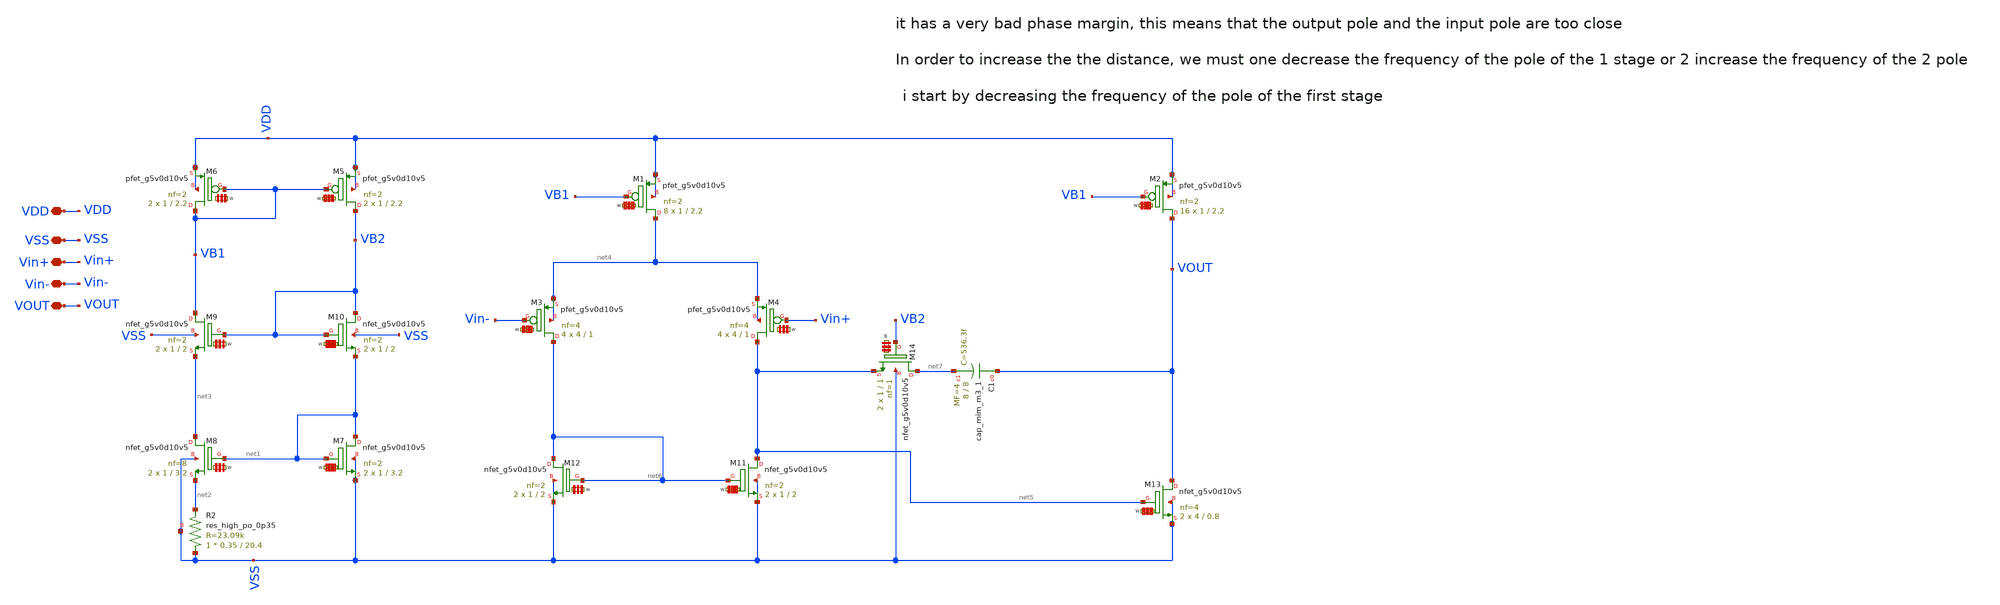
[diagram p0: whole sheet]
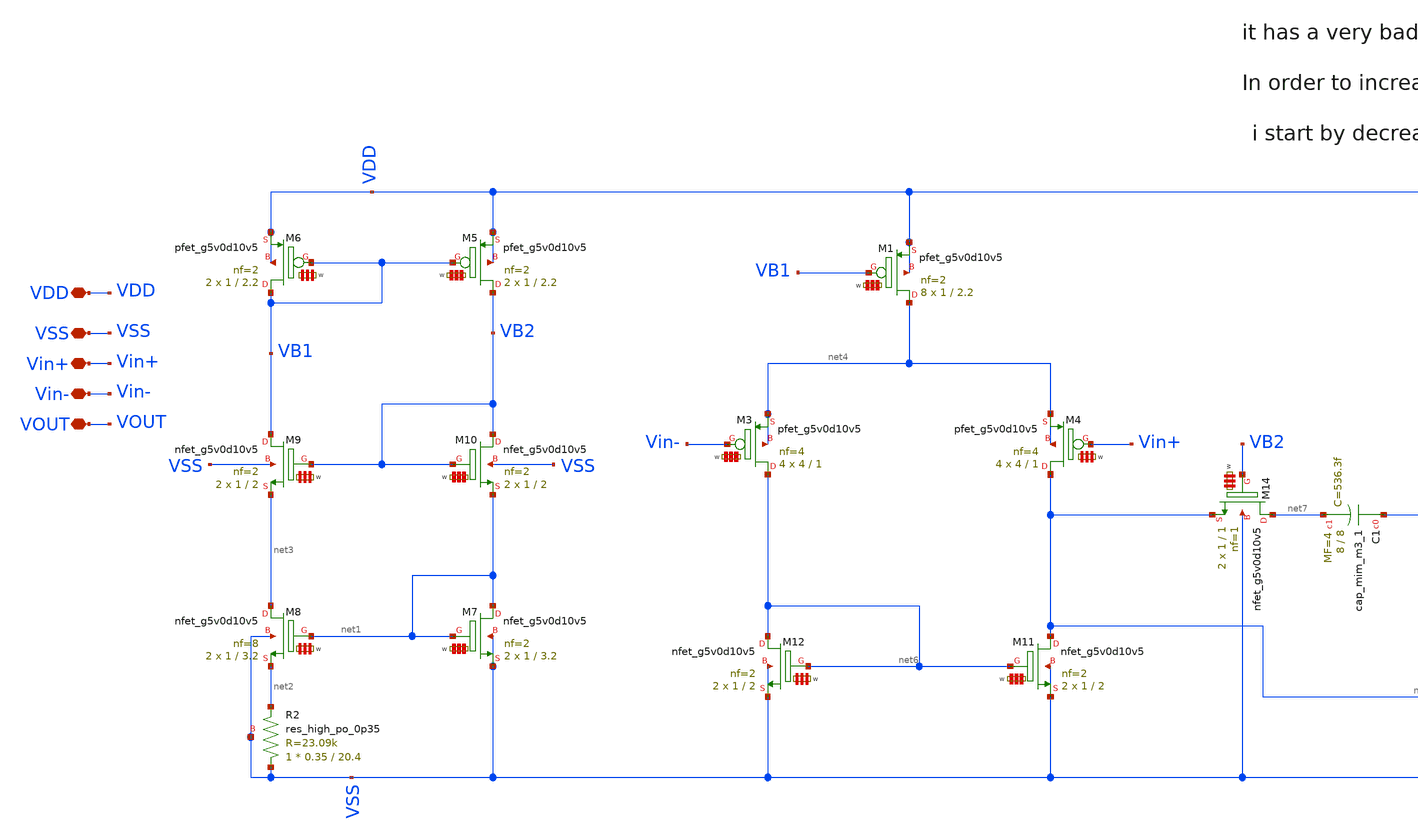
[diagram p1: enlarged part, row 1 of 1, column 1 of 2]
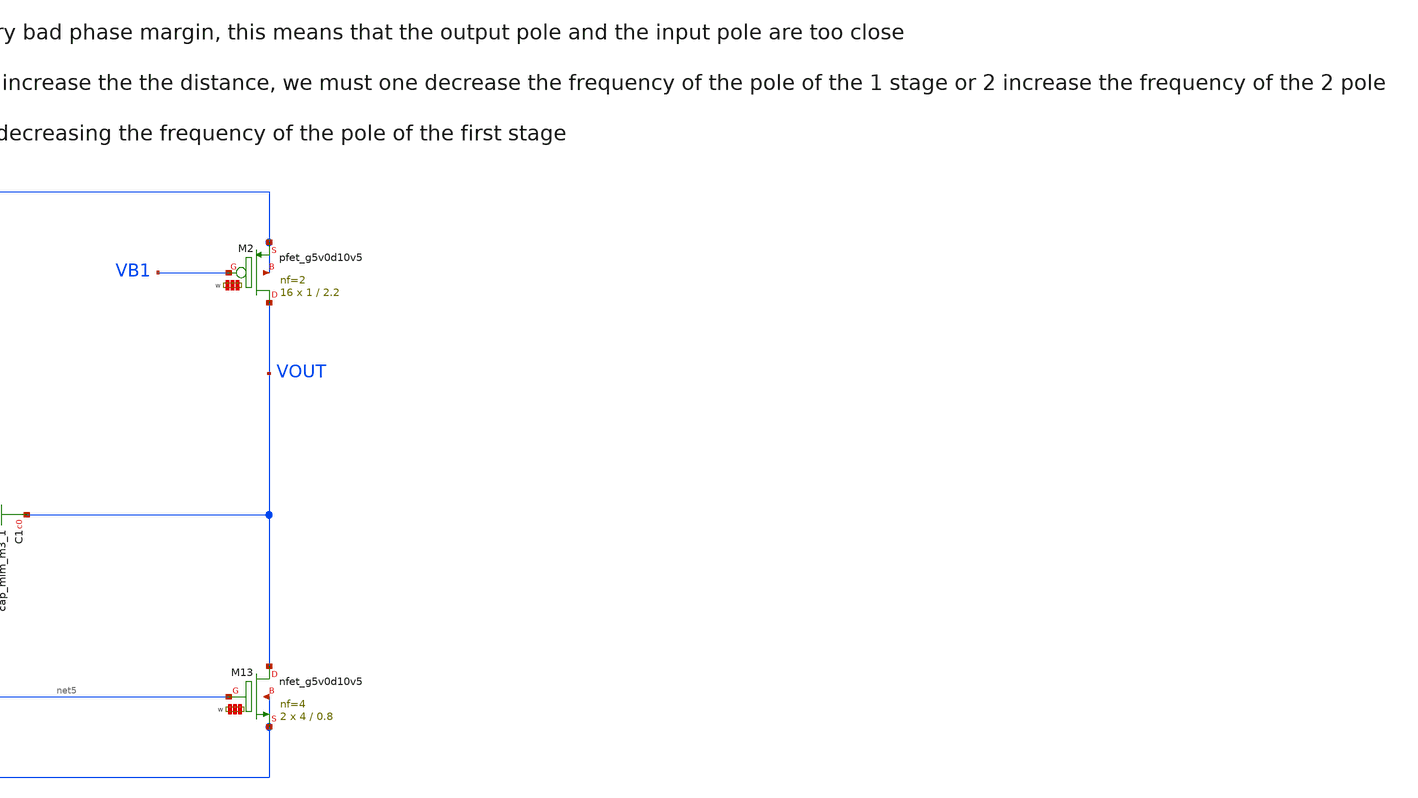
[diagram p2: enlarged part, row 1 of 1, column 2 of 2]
** sch_path: my_ip/LIB/Sky130A/Learning/Design_of_Two-Stage_CMOS_Operational_Amplifier_for_Fluorescence_Signal_Processing_5V/A001.sch
**.subckt A001 VDD VSS Vin+ Vin- VOUT
*.iopin VDD
*.iopin VSS
*.iopin Vin+
*.iopin Vin-
*.iopin VOUT
XM5 VB2 VB1 VDD VDD sky130_fd_pr__pfet_g5v0d10v5 L=2.2 W='1 * 2 ' nf=2 ad='int((2 + 1)/2) * 1 * 0.29'
+ as='int((2 + 2)/2) * 1 * 0.29' pd='2*int((2 + 1)/2) * (1 + 0.29)' ps='2*int((2 + 2)/2) * (1 + 0.29)'
+ nrd='0.29 / 1 / 2 ' nrs='0.29 / 1 / 2 ' sa=0 sb=0 sd=0 mult=2 m=2
XM6 VB1 VB1 VDD VDD sky130_fd_pr__pfet_g5v0d10v5 L=2.2 W='1 * 2 ' nf=2 ad='int((2 + 1)/2) * 1 * 0.29'
+ as='int((2 + 2)/2) * 1 * 0.29' pd='2*int((2 + 1)/2) * (1 + 0.29)' ps='2*int((2 + 2)/2) * (1 + 0.29)'
+ nrd='0.29 / 1 / 2 ' nrs='0.29 / 1 / 2 ' sa=0 sb=0 sd=0 mult=2 m=2
XR2 VSS net2 VSS sky130_fd_pr__res_high_po_0p35 L=20.4 mult=1 m=1
XM7 net1 net1 VSS VSS sky130_fd_pr__nfet_g5v0d10v5 L=3.2 W='1 * 2 ' nf=2 ad='int((nf+1)/2) * W / nf * 0.29'
+ as='int((nf+2)/2) * W / nf * 0.29' pd='2*int((nf+1)/2) * (W / nf + 0.29)' ps='2*int((nf+2)/2) * (W / nf + 0.29)'
+ nrd='0.29 / W ' nrs='0.29 / W ' sa=0 sb=0 sd=0 mult=2 m=2
XM8 net3 net1 net2 VSS sky130_fd_pr__nfet_g5v0d10v5 L=3.2 W='1 * 8 ' nf=8 ad='int((nf+1)/2) * W / nf * 0.29'
+ as='int((nf+2)/2) * W / nf * 0.29' pd='2*int((nf+1)/2) * (W / nf + 0.29)' ps='2*int((nf+2)/2) * (W / nf + 0.29)'
+ nrd='0.29 / W ' nrs='0.29 / W ' sa=0 sb=0 sd=0 mult=2 m=2
XM9 VB1 VB2 net3 VSS sky130_fd_pr__nfet_g5v0d10v5 L=2 W='1 * 2 ' nf=2 ad='int((nf+1)/2) * W / nf * 0.29'
+ as='int((nf+2)/2) * W / nf * 0.29' pd='2*int((nf+1)/2) * (W / nf + 0.29)' ps='2*int((nf+2)/2) * (W / nf + 0.29)'
+ nrd='0.29 / W ' nrs='0.29 / W ' sa=0 sb=0 sd=0 mult=2 m=2
XM10 VB2 VB2 net1 VSS sky130_fd_pr__nfet_g5v0d10v5 L=2 W='1 * 2 ' nf=2 ad='int((nf+1)/2) * W / nf * 0.29'
+ as='int((nf+2)/2) * W / nf * 0.29' pd='2*int((nf+1)/2) * (W / nf + 0.29)' ps='2*int((nf+2)/2) * (W / nf + 0.29)'
+ nrd='0.29 / W ' nrs='0.29 / W ' sa=0 sb=0 sd=0 mult=2 m=2
XM1 net4 VB1 VDD VDD sky130_fd_pr__pfet_g5v0d10v5 L=2.2 W='1 * 2 ' nf=2 ad='int((2 + 1)/2) * 1 * 0.29'
+ as='int((2 + 2)/2) * 1 * 0.29' pd='2*int((2 + 1)/2) * (1 + 0.29)' ps='2*int((2 + 2)/2) * (1 + 0.29)'
+ nrd='0.29 / 1 / 2 ' nrs='0.29 / 1 / 2 ' sa=0 sb=0 sd=0 mult=8 m=8
XM2 VOUT VB1 VDD VDD sky130_fd_pr__pfet_g5v0d10v5 L=2.2 W='1 * 2 ' nf=2 ad='int((2 + 1)/2) * 1 * 0.29'
+ as='int((2 + 2)/2) * 1 * 0.29' pd='2*int((2 + 1)/2) * (1 + 0.29)' ps='2*int((2 + 2)/2) * (1 + 0.29)'
+ nrd='0.29 / 1 / 2 ' nrs='0.29 / 1 / 2 ' sa=0 sb=0 sd=0 mult=16 m=16
XM3 net6 Vin- net4 net4 sky130_fd_pr__pfet_g5v0d10v5 L=1 W='4 * 4 ' nf=4 ad='int((4 + 1)/2) * 4 * 0.29'
+ as='int((4 + 2)/2) * 4 * 0.29' pd='2*int((4 + 1)/2) * (4 + 0.29)' ps='2*int((4 + 2)/2) * (4 + 0.29)'
+ nrd='0.29 / 4 / 4 ' nrs='0.29 / 4 / 4 ' sa=0 sb=0 sd=0 mult=4 m=4
XM4 net5 Vin+ net4 net4 sky130_fd_pr__pfet_g5v0d10v5 L=1 W='4 * 4 ' nf=4 ad='int((4 + 1)/2) * 4 * 0.29'
+ as='int((4 + 2)/2) * 4 * 0.29' pd='2*int((4 + 1)/2) * (4 + 0.29)' ps='2*int((4 + 2)/2) * (4 + 0.29)'
+ nrd='0.29 / 4 / 4 ' nrs='0.29 / 4 / 4 ' sa=0 sb=0 sd=0 mult=4 m=4
XM11 net5 net6 VSS VSS sky130_fd_pr__nfet_g5v0d10v5 L=2 W='1 * 2 ' nf=2 ad='int((nf+1)/2) * W / nf * 0.29'
+ as='int((nf+2)/2) * W / nf * 0.29' pd='2*int((nf+1)/2) * (W / nf + 0.29)' ps='2*int((nf+2)/2) * (W / nf + 0.29)'
+ nrd='0.29 / W ' nrs='0.29 / W ' sa=0 sb=0 sd=0 mult=2 m=2
XM12 net6 net6 VSS VSS sky130_fd_pr__nfet_g5v0d10v5 L=2 W='1 * 2 ' nf=2 ad='int((nf+1)/2) * W / nf * 0.29'
+ as='int((nf+2)/2) * W / nf * 0.29' pd='2*int((nf+1)/2) * (W / nf + 0.29)' ps='2*int((nf+2)/2) * (W / nf + 0.29)'
+ nrd='0.29 / W ' nrs='0.29 / W ' sa=0 sb=0 sd=0 mult=2 m=2
XM13 VOUT net5 VSS VSS sky130_fd_pr__nfet_g5v0d10v5 L=0.8 W='4 * 4 ' nf=4 ad='int((nf+1)/2) * W / nf * 0.29'
+ as='int((nf+2)/2) * W / nf * 0.29' pd='2*int((nf+1)/2) * (W / nf + 0.29)' ps='2*int((nf+2)/2) * (W / nf + 0.29)'
+ nrd='0.29 / W ' nrs='0.29 / W ' sa=0 sb=0 sd=0 mult=2 m=2
XM14 net7 VB2 net5 VSS sky130_fd_pr__nfet_g5v0d10v5 L=1 W='1 * 1 ' nf=1 ad='int((nf+1)/2) * W / nf * 0.29'
+ as='int((nf+2)/2) * W / nf * 0.29' pd='2*int((nf+1)/2) * (W / nf + 0.29)' ps='2*int((nf+2)/2) * (W / nf + 0.29)'
+ nrd='0.29 / W ' nrs='0.29 / W ' sa=0 sb=0 sd=0 mult=2 m=2
XC1 VOUT net7 sky130_fd_pr__cap_mim_m3_1 W=8 L=8 MF=4 m=4
**.ends
.end
